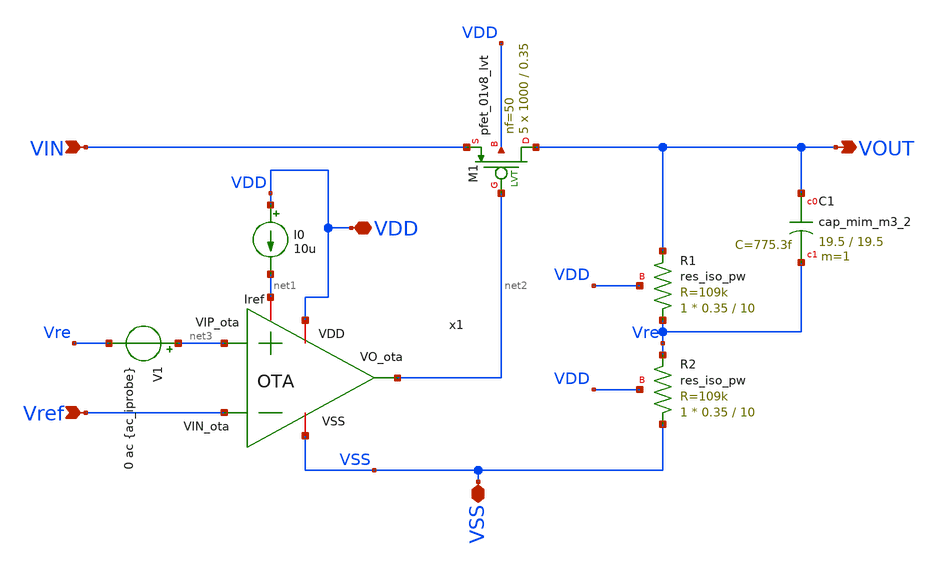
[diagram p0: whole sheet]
** sch_path: xschem/LDO.sch
**.subckt LDO VIN VDD VOUT Vref VSS
*.ipin VIN
*.iopin VDD
*.opin VOUT
*.ipin Vref
*.iopin VSS
x1 VDD net2 Vref net3 net1 VSS OTA
I0 VDD net1 10u
XM1 VOUT net2 VIN VDD sky130_fd_pr__pfet_01v8_lvt L=0.35 W=1000 nf=50 ad='int((50 + 1)/2) * 1000 / 50 * 0.29'
+ as='int((50 + 2)/2) * 1000 / 50 * 0.29' pd='2*int((50 + 1)/2) * (1000 / 50 + 0.29)' ps='2*int((50 + 2)/2) * (1000 / 50 + 0.29)'
+ nrd='0.29 / 1000 ' nrs='0.29 / 1000 ' sa=0 sb=0 sd=0 mult=5 m=5
XR1 Vre VOUT VDD sky130_fd_pr__res_iso_pw W=0.35 L=10 m=1
XR2 VSS Vre VDD sky130_fd_pr__res_iso_pw W=0.35 L=10 m=1
V1 net3 Vre 0 ac {ac_iprobe}
XC1 VOUT Vre sky130_fd_pr__cap_mim_m3_2 W=19.5 L=19.5 MF=1 m=1
**.ends

* expanding   symbol:  /foss/designs/LDO-sky130/xschem/OTA.sym # of pins=6
** sym_path: xschem/OTA.sym
** sch_path: xschem/OTA.sch
.subckt OTA VDD VO_ota VIN_ota VIP_ota Iref VSS
*.ipin VIN_ota
*.opin VO_ota
*.iopin Iref
*.iopin VSS
*.iopin VDD
*.ipin VIP_ota
XMr Iref Iref VSS VSS sky130_fd_pr__nfet_01v8 L=0.5 W=0.5 nf=1 ad='int((1 + 1)/2) * 0.5 / 1 * 0.29' as='int((1 + 2)/2) * 0.5 / 1 * 0.29'
+ pd='2*int((1 + 1)/2) * (0.5 / 1 + 0.29)' ps='2*int((1 + 2)/2) * (0.5 / 1 + 0.29)' nrd='0.29 / 0.5 ' nrs='0.29 / 0.5 '
+ sa=0 sb=0 sd=0 mult=1 m=1
XMo VO_ota VO_ota1 VDD VDD sky130_fd_pr__pfet_01v8 L=0.5 W=20 nf=1 ad='int((1 + 1)/2) * 20 / 1 * 0.29'
+ as='int((1 + 2)/2) * 20 / 1 * 0.29' pd='2*int((1 + 1)/2) * (20 / 1 + 0.29)' ps='2*int((1 + 2)/2) * (20 / 1 + 0.29)'
+ nrd='0.29 / 20 ' nrs='0.29 / 20 ' sa=0 sb=0 sd=0 mult=1 m=1
XMrc1 Vtail Iref VSS VSS sky130_fd_pr__nfet_01v8 L=0.5 W=2 nf=1 ad='int((1 + 1)/2) * 2 / 1 * 0.29' as='int((1 + 2)/2) * 2 / 1 * 0.29'
+ pd='2*int((1 + 1)/2) * (2 / 1 + 0.29)' ps='2*int((1 + 2)/2) * (2 / 1 + 0.29)' nrd='0.29 / 2 ' nrs='0.29 / 2 '
+ sa=0 sb=0 sd=0 mult=1 m=1
XMc2 VO_ota Iref VSS VSS sky130_fd_pr__nfet_01v8 L=0.5 W=1 nf=1 ad='int((1 + 1)/2) * 1 / 1 * 0.29' as='int((1 + 2)/2) * 1 / 1 * 0.29'
+ pd='2*int((1 + 1)/2) * (1 / 1 + 0.29)' ps='2*int((1 + 2)/2) * (1 / 1 + 0.29)' nrd='0.29 / 1 ' nrs='0.29 / 1 '
+ sa=0 sb=0 sd=0 mult=1 m=1
XMn VGP VIN_ota Vtail VSS sky130_fd_pr__nfet_01v8 L=0.5 W=40 nf=1 ad='int((1 + 1)/2) * 40 / 1 * 0.29'
+ as='int((1 + 2)/2) * 40 / 1 * 0.29' pd='2*int((1 + 1)/2) * (40 / 1 + 0.29)' ps='2*int((1 + 2)/2) * (40 / 1 + 0.29)'
+ nrd='0.29 / 40 ' nrs='0.29 / 40 ' sa=0 sb=0 sd=0 mult=1 m=1
XMp VO_ota1 VIP_ota Vtail VSS sky130_fd_pr__nfet_01v8 L=0.5 W=40 nf=1 ad='int((1 + 1)/2) * 40 / 1 * 0.29'
+ as='int((1 + 2)/2) * 40 / 1 * 0.29' pd='2*int((1 + 1)/2) * (40 / 1 + 0.29)' ps='2*int((1 + 2)/2) * (40 / 1 + 0.29)'
+ nrd='0.29 / 40 ' nrs='0.29 / 40 ' sa=0 sb=0 sd=0 mult=1 m=1
XMpr VO_ota1 VGP VDD VDD sky130_fd_pr__pfet_01v8 L=0.5 W=40 nf=1 ad='int((1 + 1)/2) * 40 / 1 * 0.29'
+ as='int((1 + 2)/2) * 40 / 1 * 0.29' pd='2*int((1 + 1)/2) * (40 / 1 + 0.29)' ps='2*int((1 + 2)/2) * (40 / 1 + 0.29)'
+ nrd='0.29 / 40 ' nrs='0.29 / 40 ' sa=0 sb=0 sd=0 mult=1 m=1
XMnr VGP VGP VDD VDD sky130_fd_pr__pfet_01v8 L=0.5 W=40 nf=1 ad='int((1 + 1)/2) * 40 / 1 * 0.29' as='int((1 + 2)/2) * 40 / 1 * 0.29'
+ pd='2*int((1 + 1)/2) * (40 / 1 + 0.29)' ps='2*int((1 + 2)/2) * (40 / 1 + 0.29)' nrd='0.29 / 40 ' nrs='0.29 / 40 '
+ sa=0 sb=0 sd=0 mult=1 m=1
XR1 VO_ota1 net1 VDD sky130_fd_pr__res_high_po W=0.35 L=360 mult=1 m=1
XC1 VO_ota net1 sky130_fd_pr__cap_mim_m3_2 W=50 L=50 MF=1 m=1
.ends

.end
